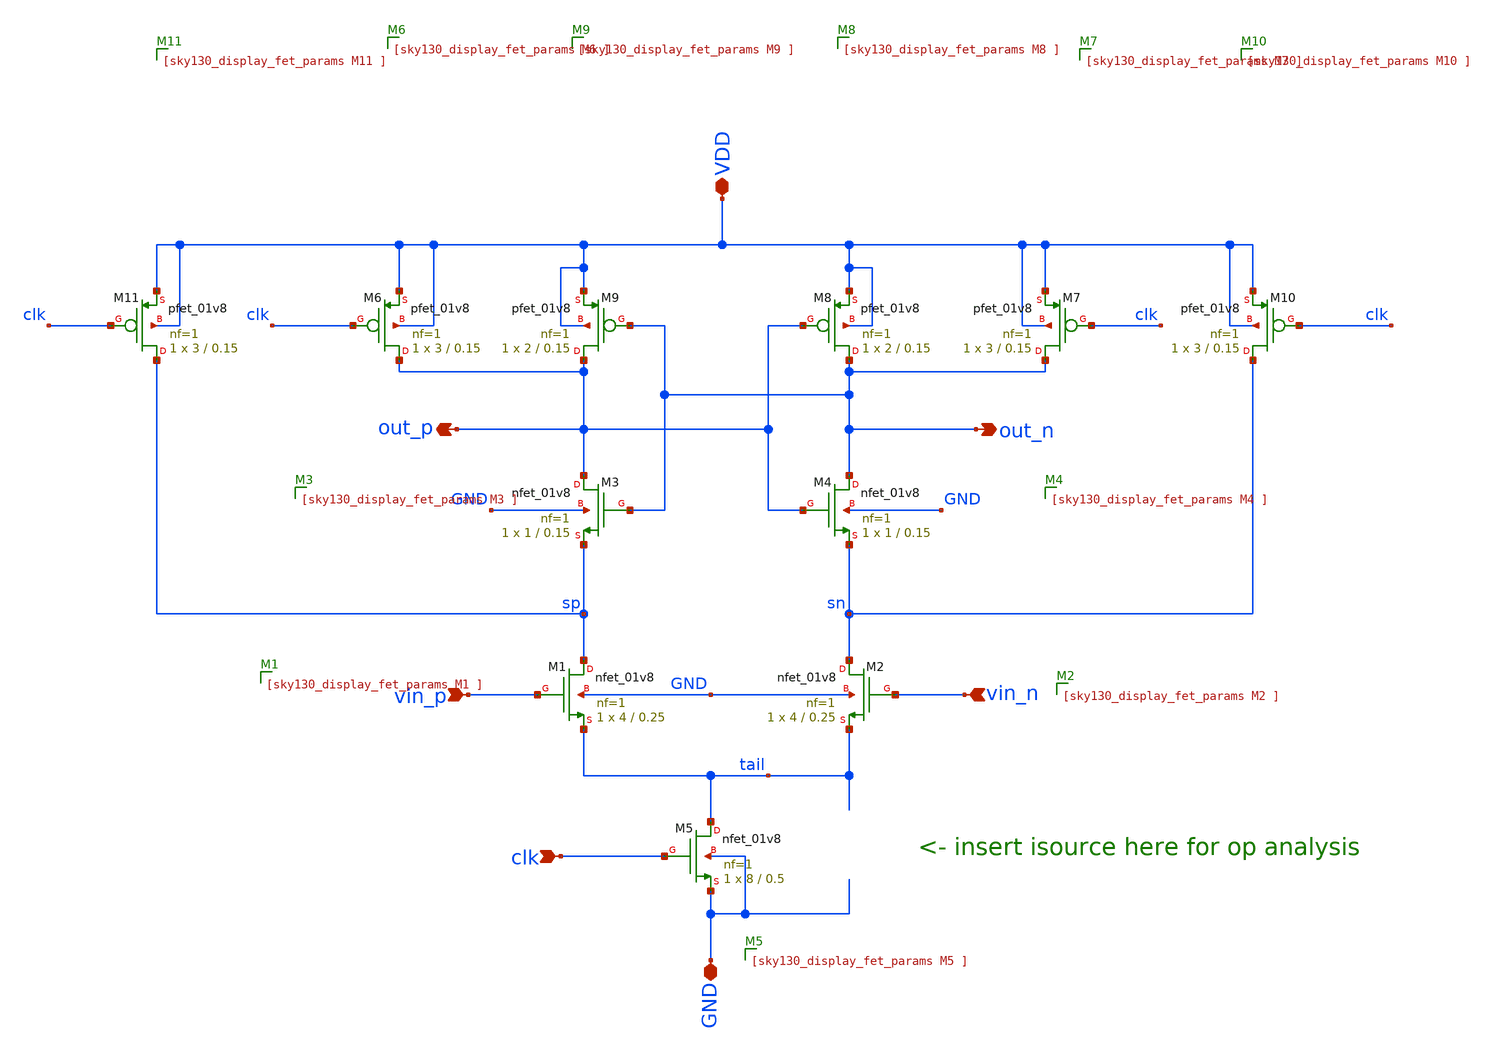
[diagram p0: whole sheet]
** sch_path: 05_mixed_signal/soluzioni/lab03/xschem/strongarm.sch
**.subckt strongarm vin_p vin_n clk out_n out_p VDD GND
*.ipin vin_p
*.ipin vin_n
*.ipin clk
*.opin out_n
*.opin out_p
*.iopin VDD
*.iopin GND
XM1 sp vin_p tail GND sky130_fd_pr__nfet_01v8 L=0.25 W=4 nf=1 ad='int((1 + 1)/2) * 4 / 1 * 0.29' as='int((1 + 2)/2) * 4 / 1 * 0.29'
+ pd='2*int((1 + 1)/2) * (4 / 1 + 0.29)' ps='2*int((1 + 2)/2) * (4 / 1 + 0.29)' nrd='0.29 / 4 ' nrs='0.29 / 4 '
+ sa=0 sb=0 sd=0 mult=1 m=1
XM2 sn vin_n tail GND sky130_fd_pr__nfet_01v8 L=0.25 W=4 nf=1 ad='int((1 + 1)/2) * 4 / 1 * 0.29' as='int((1 + 2)/2) * 4 / 1 * 0.29'
+ pd='2*int((1 + 1)/2) * (4 / 1 + 0.29)' ps='2*int((1 + 2)/2) * (4 / 1 + 0.29)' nrd='0.29 / 4 ' nrs='0.29 / 4 '
+ sa=0 sb=0 sd=0 mult=1 m=1
XM3 out_p out_n sp GND sky130_fd_pr__nfet_01v8 L=0.15 W=1 nf=1 ad='int((1 + 1)/2) * 1 / 1 * 0.29' as='int((1 + 2)/2) * 1 / 1 * 0.29'
+ pd='2*int((1 + 1)/2) * (1 / 1 + 0.29)' ps='2*int((1 + 2)/2) * (1 / 1 + 0.29)' nrd='0.29 / 1 ' nrs='0.29 / 1 '
+ sa=0 sb=0 sd=0 mult=1 m=1
XM4 out_n out_p sn GND sky130_fd_pr__nfet_01v8 L=0.15 W=1 nf=1 ad='int((1 + 1)/2) * 1 / 1 * 0.29' as='int((1 + 2)/2) * 1 / 1 * 0.29'
+ pd='2*int((1 + 1)/2) * (1 / 1 + 0.29)' ps='2*int((1 + 2)/2) * (1 / 1 + 0.29)' nrd='0.29 / 1 ' nrs='0.29 / 1 '
+ sa=0 sb=0 sd=0 mult=1 m=1
XM5 tail clk GND GND sky130_fd_pr__nfet_01v8 L=0.5 W=8 nf=1 ad='int((1 + 1)/2) * 8 / 1 * 0.29' as='int((1 + 2)/2) * 8 / 1 * 0.29'
+ pd='2*int((1 + 1)/2) * (8 / 1 + 0.29)' ps='2*int((1 + 2)/2) * (8 / 1 + 0.29)' nrd='0.29 / 8 ' nrs='0.29 / 8 '
+ sa=0 sb=0 sd=0 mult=1 m=1
XM6 out_p clk VDD VDD sky130_fd_pr__pfet_01v8 L=0.15 W=3 nf=1 ad='int((1 + 1)/2) * 3 / 1 * 0.29' as='int((1 + 2)/2) * 3 / 1 * 0.29'
+ pd='2*int((1 + 1)/2) * (3 / 1 + 0.29)' ps='2*int((1 + 2)/2) * (3 / 1 + 0.29)' nrd='0.29 / 3 ' nrs='0.29 / 3 '
+ sa=0 sb=0 sd=0 mult=1 m=1
XM7 out_n clk VDD VDD sky130_fd_pr__pfet_01v8 L=0.15 W=3 nf=1 ad='int((1 + 1)/2) * 3 / 1 * 0.29' as='int((1 + 2)/2) * 3 / 1 * 0.29'
+ pd='2*int((1 + 1)/2) * (3 / 1 + 0.29)' ps='2*int((1 + 2)/2) * (3 / 1 + 0.29)' nrd='0.29 / 3 ' nrs='0.29 / 3 '
+ sa=0 sb=0 sd=0 mult=1 m=1
XM8 out_n out_p VDD VDD sky130_fd_pr__pfet_01v8 L=0.15 W=2 nf=1 ad='int((1 + 1)/2) * 2 / 1 * 0.29' as='int((1 + 2)/2) * 2 / 1 * 0.29'
+ pd='2*int((1 + 1)/2) * (2 / 1 + 0.29)' ps='2*int((1 + 2)/2) * (2 / 1 + 0.29)' nrd='0.29 / 2 ' nrs='0.29 / 2 '
+ sa=0 sb=0 sd=0 mult=1 m=1
XM9 out_p out_n VDD VDD sky130_fd_pr__pfet_01v8 L=0.15 W=2 nf=1 ad='int((1 + 1)/2) * 2 / 1 * 0.29' as='int((1 + 2)/2) * 2 / 1 * 0.29'
+ pd='2*int((1 + 1)/2) * (2 / 1 + 0.29)' ps='2*int((1 + 2)/2) * (2 / 1 + 0.29)' nrd='0.29 / 2 ' nrs='0.29 / 2 '
+ sa=0 sb=0 sd=0 mult=1 m=1
XM10 sn clk VDD VDD sky130_fd_pr__pfet_01v8 L=0.15 W=3 nf=1 ad='int((1 + 1)/2) * 3 / 1 * 0.29' as='int((1 + 2)/2) * 3 / 1 * 0.29'
+ pd='2*int((1 + 1)/2) * (3 / 1 + 0.29)' ps='2*int((1 + 2)/2) * (3 / 1 + 0.29)' nrd='0.29 / 3 ' nrs='0.29 / 3 '
+ sa=0 sb=0 sd=0 mult=1 m=1
XM11 sp clk VDD VDD sky130_fd_pr__pfet_01v8 L=0.15 W=3 nf=1 ad='int((1 + 1)/2) * 3 / 1 * 0.29' as='int((1 + 2)/2) * 3 / 1 * 0.29'
+ pd='2*int((1 + 1)/2) * (3 / 1 + 0.29)' ps='2*int((1 + 2)/2) * (3 / 1 + 0.29)' nrd='0.29 / 3 ' nrs='0.29 / 3 '
+ sa=0 sb=0 sd=0 mult=1 m=1
**.ends
.end
